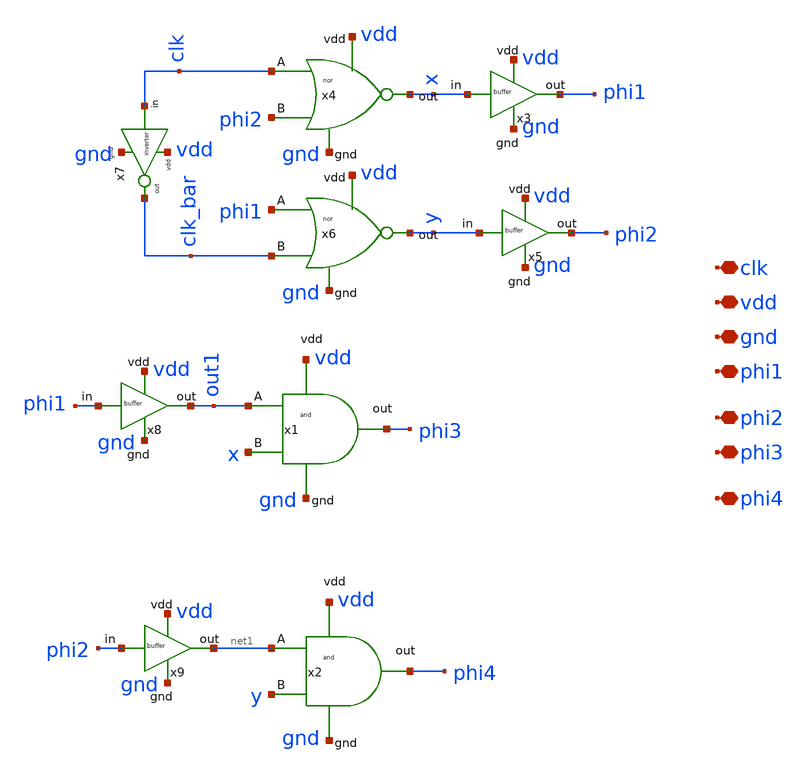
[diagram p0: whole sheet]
** sch_path: Clock_gen_using_transistor_hv/pulse_gen_circuit.sch
**.subckt pulse_gen_circuit vdd gnd phi1 phi2 phi3 phi4 clk
*.iopin vdd
*.iopin gnd
*.iopin phi1
*.iopin phi2
*.iopin phi3
*.iopin phi4
*.iopin clk
x1 vdd x out1 gnd phi3 and
x2 vdd y net1 gnd phi4 and
x4 vdd phi2 clk gnd x nor
x6 vdd clk_bar phi1 gnd y nor
x7 clk clk_bar vdd gnd inverter
x8 phi1 out1 vdd gnd buffer
x9 phi2 net1 vdd gnd buffer
x3 x phi1 vdd gnd buffer
x5 y phi2 vdd gnd buffer
**.ends

* expanding   symbol:
*+  /home/designer/shared/unicass_2026/Design_Files/github_clone_circuit_/UNI-CASS_Project_2025_IIT_DH/Clock_gen_using_transistor_hv/and.sym # of pins=5
** sym_path: /home/designer/shared/unicass_2026/Design_Files/github_clone_circuit_/UNI-CASS_Project_2025_IIT_DH/Clock_gen_using_transistor_hv/and.sym
** sch_path: /home/designer/shared/unicass_2026/Design_Files/github_clone_circuit_/UNI-CASS_Project_2025_IIT_DH/Clock_gen_using_transistor_hv/and.sch
.subckt and vdd B A gnd out
*.iopin vdd
*.iopin B
*.iopin A
*.iopin gnd
*.iopin out
XM3 net1 A vdd vdd sg13_hv_pmos w=0.3u l=0.45u ng=1 m=1 mm_ok=1
XM1 net2 B gnd gnd sg13_hv_nmos w=0.3u l=0.45u ng=1 m=1 mm_ok=1
XM2 net1 A net2 net2 sg13_hv_nmos w=0.3u l=0.45u ng=1 m=1 mm_ok=1
XM4 net1 B vdd vdd sg13_hv_pmos w=0.3u l=0.45u ng=1 m=1 mm_ok=1
XM5 out net1 vdd vdd sg13_hv_pmos w=0.3u l=0.45u ng=1 m=1 mm_ok=1
XM6 out net1 gnd gnd sg13_hv_nmos w=0.3u l=0.45u ng=1 m=1 mm_ok=1
.ends


* expanding   symbol:
*+  /home/designer/shared/unicass_2026/Design_Files/github_clone_circuit_/UNI-CASS_Project_2025_IIT_DH/Clock_gen_using_transistor_hv/nor.sym # of pins=5
** sym_path: /home/designer/shared/unicass_2026/Design_Files/github_clone_circuit_/UNI-CASS_Project_2025_IIT_DH/Clock_gen_using_transistor_hv/nor.sym
** sch_path: /home/designer/shared/unicass_2026/Design_Files/github_clone_circuit_/UNI-CASS_Project_2025_IIT_DH/Clock_gen_using_transistor_hv/nor.sch
.subckt nor vdd B A gnd out
*.iopin vdd
*.iopin B
*.iopin A
*.iopin gnd
*.iopin out
XM3 net1 A vdd vdd sg13_hv_pmos w=0.3u l=0.45u ng=1 m=1 mm_ok=1
XM1 out B gnd gnd sg13_hv_nmos w=0.3u l=0.45u ng=1 m=1 mm_ok=1
XM2 out A gnd gnd sg13_hv_nmos w=0.3u l=0.45u ng=1 m=1 mm_ok=1
XM4 out B net1 net1 sg13_hv_pmos w=0.3u l=0.45u ng=1 m=1 mm_ok=1
.ends


* expanding   symbol:
*+  /home/designer/shared/unicass_2026/Design_Files/github_clone_circuit_/UNI-CASS_Project_2025_IIT_DH/Clock_gen_using_transistor_hv/inverter.sym # of pins=4
** sym_path: /home/designer/shared/unicass_2026/Design_Files/github_clone_circuit_/UNI-CASS_Project_2025_IIT_DH/Clock_gen_using_transistor_hv/inverter.sym
** sch_path: /home/designer/shared/unicass_2026/Design_Files/github_clone_circuit_/UNI-CASS_Project_2025_IIT_DH/Clock_gen_using_transistor_hv/inverter.sch
.subckt inverter in out vdd gnd
*.iopin in
*.iopin vdd
*.iopin out
*.iopin gnd
XM3 out in vdd vdd sg13_hv_pmos w=2u l=2u ng=1 m=1 mm_ok=1
XM1 out in gnd gnd sg13_hv_nmos w=1u l=1u ng=1 m=1 mm_ok=1
.ends


* expanding   symbol:
*+  /home/designer/shared/unicass_2026/Design_Files/github_clone_circuit_/UNI-CASS_Project_2025_IIT_DH/Clock_gen_using_transistor_hv/buffer.sym # of pins=4
** sym_path: /home/designer/shared/unicass_2026/Design_Files/github_clone_circuit_/UNI-CASS_Project_2025_IIT_DH/Clock_gen_using_transistor_hv/buffer.sym
** sch_path: /home/designer/shared/unicass_2026/Design_Files/github_clone_circuit_/UNI-CASS_Project_2025_IIT_DH/Clock_gen_using_transistor_hv/buffer.sch
.subckt buffer in out vdd gnd
*.iopin in
*.iopin out
*.iopin vdd
*.iopin gnd
x1 in net1 vdd gnd inverter
x2 net1 net2 vdd gnd inverter
x3 net2 net3 vdd gnd inverter
x4 net3 out vdd gnd inverter
XC1 net1 gnd net4 cap_rfcmim w=7.0e-6 l=7.0e-6 wfeed=5.0e-6 m=1 mm_ok=1
.ends

.end
